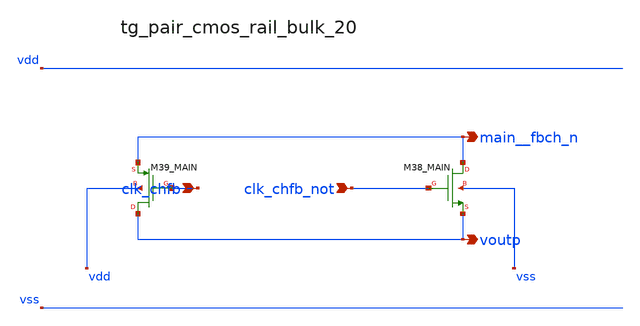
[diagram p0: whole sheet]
** sch_path: analog-db/raw/ia_004_fan_chopper_rrl/hier/blocks/tg_pair_cmos_rail_bulk_20.sch
**.subckt tg_pair_cmos_rail_bulk_20 clk_chfb clk_chfb_not main__fbch_n voutp
*.ipin clk_chfb
*.ipin clk_chfb_not
*.opin main__fbch_n
*.opin voutp
XM38_MAIN main__fbch_n clk_chfb_not voutp vss sg13_lv_nmos w=x_dut_xm38_main_w l=x_dut_xm38_main_l
+ ng=1 m=x_dut_xm38_main_m
XM39_MAIN voutp clk_chfb main__fbch_n vdd sg13_lv_pmos w=x_dut_xm39_main_w l=x_dut_xm39_main_l ng=1
+ m=x_dut_xm39_main_m
**.ends
.end
